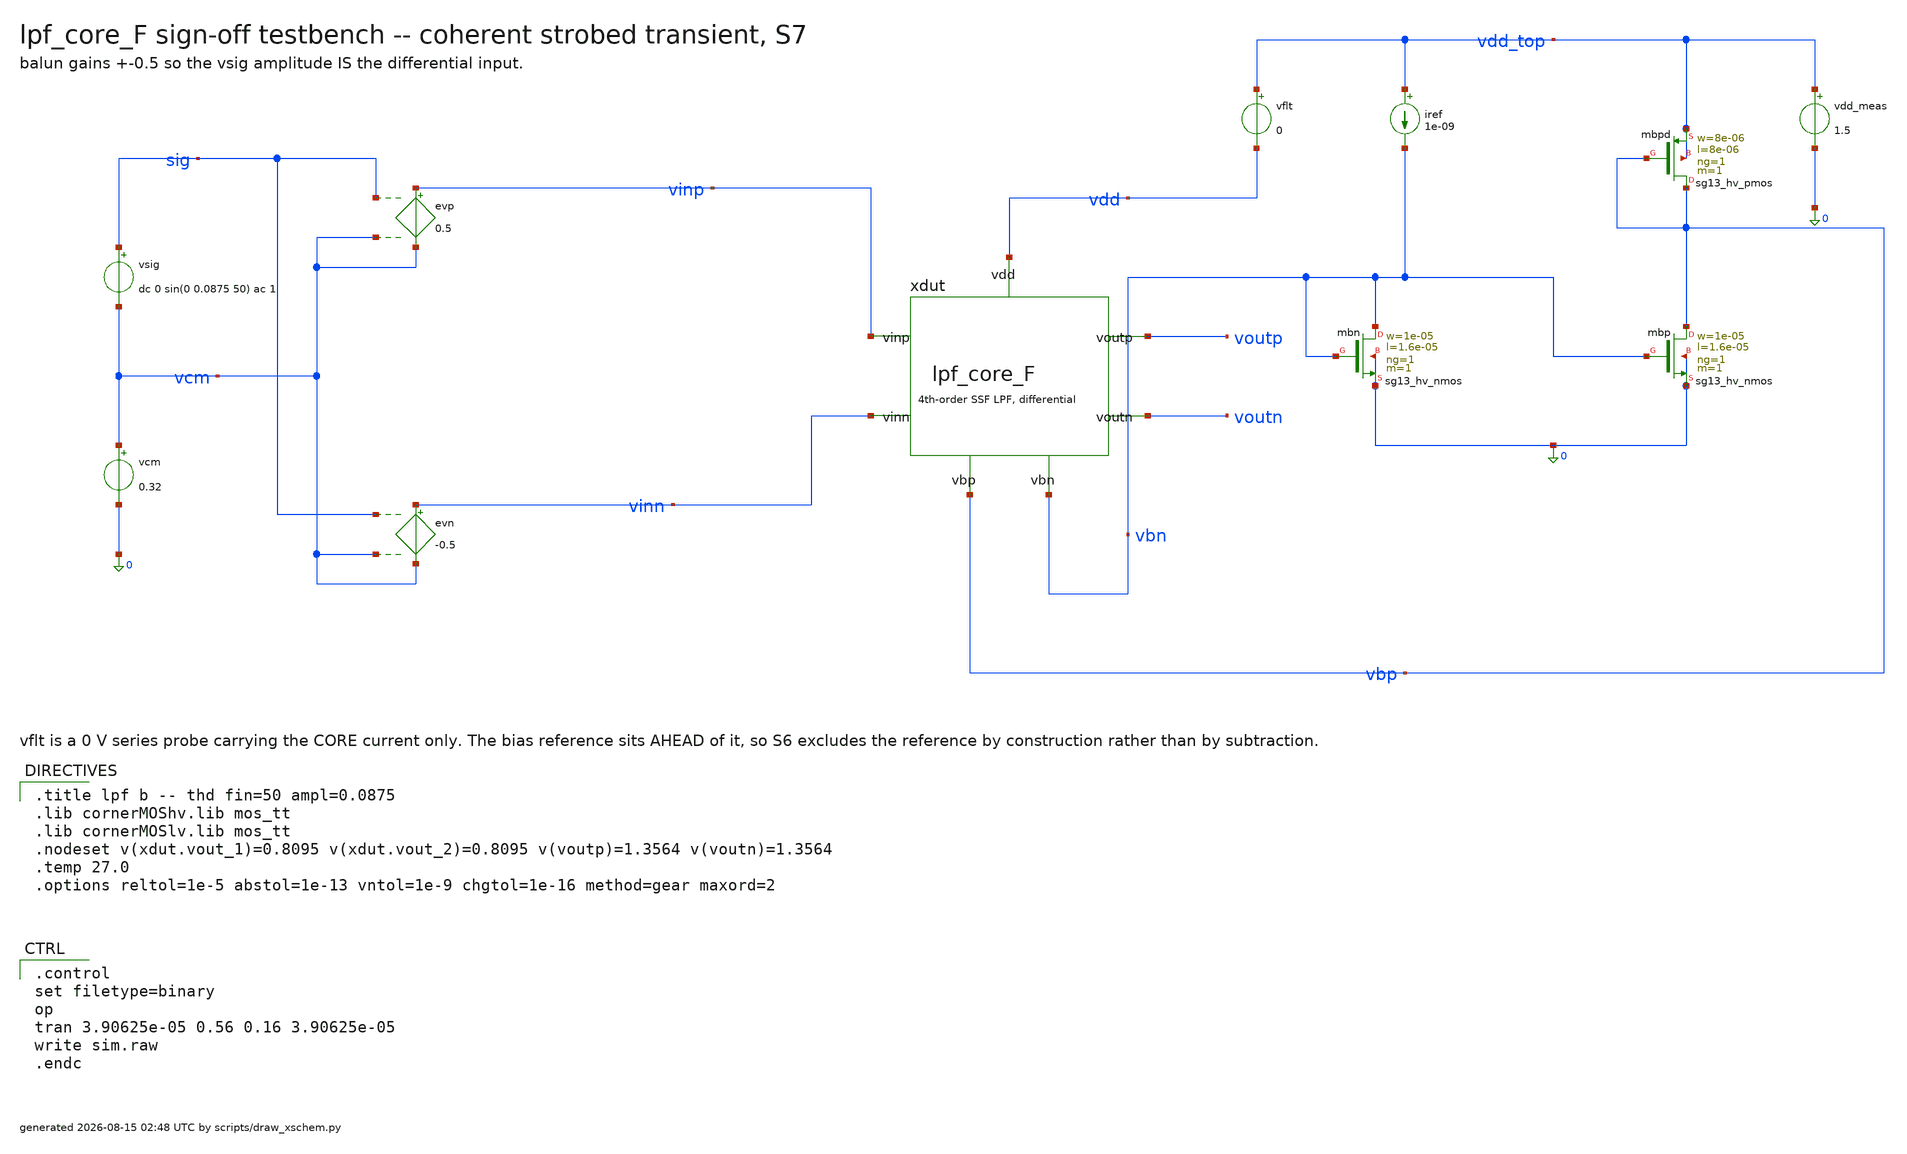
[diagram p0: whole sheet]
** sch_path: signoff/pre-pvt/F-minnoise/lpf_tb_F_thd.sch
**.subckt lpf_tb_F_thd
vsig sig vcm dc 0 sin(0 0.0875 50) ac 1
vcm vcm 0 0.32
evp vinp vcm sig vcm 0.5
evn vinn vcm sig vcm -0.5
xdut vinp vinn voutp voutn vbn vbp vdd lpf_core_F
vflt vdd_top vdd 0
vdd_meas vdd_top 0 1.5
iref vdd_top vbn 1e-09
Xmbn vbn vbn 0 0 sg13_hv_nmos w=1e-05 l=1.6e-05 ng=1 m=1 mm_ok=1
Xmbp vbp vbn 0 0 sg13_hv_nmos w=1e-05 l=1.6e-05 ng=1 m=1 mm_ok=1
Xmbpd vbp vbp vdd_top vdd_top sg13_hv_pmos w=8e-06 l=8e-06 ng=1 m=1 mm_ok=1
**** begin user architecture code

.title lpf b -- thd fin=50 ampl=0.0875
.lib cornerMOShv.lib mos_tt
.lib cornerMOSlv.lib mos_tt
.nodeset v(xdut.vout_1)=0.8095 v(xdut.vout_2)=0.8095 v(voutp)=1.3564 v(voutn)=1.3564
.temp 27.0
.options reltol=1e-5 abstol=1e-13 vntol=1e-9 chgtol=1e-16 method=gear maxord=2


.control
set filetype=binary
op
tran 3.90625e-05 0.56 0.16 3.90625e-05
write sim.raw
.endc

**** end user architecture code
**.ends
.end
